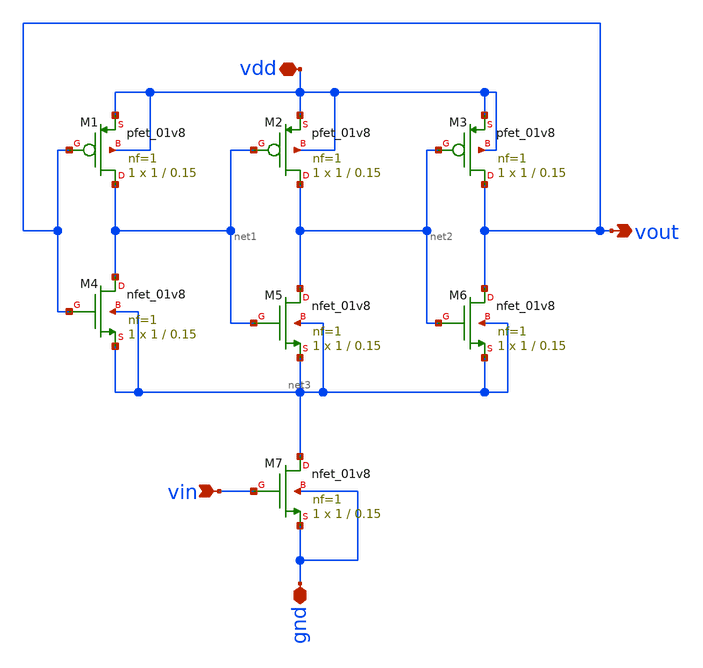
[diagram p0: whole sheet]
** sch_path: Neuron/voltContrOsc/sch/voltContrOsc.sch
**.subckt voltContrOsc gnd vdd vin vout
*.iopin gnd
*.iopin vdd
*.ipin vin
*.opin vout
XM1 net1 vout vdd vdd sky130_fd_pr__pfet_01v8 L=0.15 W=1 nf=1 ad='int((nf+1)/2) * W/nf * 0.29' as='int((nf+2)/2) * W/nf * 0.29'
+ pd='2*int((nf+1)/2) * (W/nf + 0.29)' ps='2*int((nf+2)/2) * (W/nf + 0.29)' nrd='0.29 / W' nrs='0.29 / W'
+ sa=0 sb=0 sd=0 mult=1 m=1
XM2 net2 net1 vdd vdd sky130_fd_pr__pfet_01v8 L=0.15 W=1 nf=1 ad='int((nf+1)/2) * W/nf * 0.29' as='int((nf+2)/2) * W/nf * 0.29'
+ pd='2*int((nf+1)/2) * (W/nf + 0.29)' ps='2*int((nf+2)/2) * (W/nf + 0.29)' nrd='0.29 / W' nrs='0.29 / W'
+ sa=0 sb=0 sd=0 mult=1 m=1
XM3 vout net2 vdd vdd sky130_fd_pr__pfet_01v8 L=0.15 W=1 nf=1 ad='int((nf+1)/2) * W/nf * 0.29' as='int((nf+2)/2) * W/nf * 0.29'
+ pd='2*int((nf+1)/2) * (W/nf + 0.29)' ps='2*int((nf+2)/2) * (W/nf + 0.29)' nrd='0.29 / W' nrs='0.29 / W'
+ sa=0 sb=0 sd=0 mult=1 m=1
XM4 net1 vout net3 net3 sky130_fd_pr__nfet_01v8 L=0.15 W=1 nf=1 ad='int((nf+1)/2) * W/nf * 0.29' as='int((nf+2)/2) * W/nf * 0.29'
+ pd='2*int((nf+1)/2) * (W/nf + 0.29)' ps='2*int((nf+2)/2) * (W/nf + 0.29)' nrd='0.29 / W' nrs='0.29 / W'
+ sa=0 sb=0 sd=0 mult=1 m=1
XM5 net2 net1 net3 net3 sky130_fd_pr__nfet_01v8 L=0.15 W=1 nf=1 ad='int((nf+1)/2) * W/nf * 0.29' as='int((nf+2)/2) * W/nf * 0.29'
+ pd='2*int((nf+1)/2) * (W/nf + 0.29)' ps='2*int((nf+2)/2) * (W/nf + 0.29)' nrd='0.29 / W' nrs='0.29 / W'
+ sa=0 sb=0 sd=0 mult=1 m=1
XM6 vout net2 net3 net3 sky130_fd_pr__nfet_01v8 L=0.15 W=1 nf=1 ad='int((nf+1)/2) * W/nf * 0.29' as='int((nf+2)/2) * W/nf * 0.29'
+ pd='2*int((nf+1)/2) * (W/nf + 0.29)' ps='2*int((nf+2)/2) * (W/nf + 0.29)' nrd='0.29 / W' nrs='0.29 / W'
+ sa=0 sb=0 sd=0 mult=1 m=1
XM7 net3 vin gnd gnd sky130_fd_pr__nfet_01v8 L=0.15 W=1 nf=1 ad='int((nf+1)/2) * W/nf * 0.29' as='int((nf+2)/2) * W/nf * 0.29'
+ pd='2*int((nf+1)/2) * (W/nf + 0.29)' ps='2*int((nf+2)/2) * (W/nf + 0.29)' nrd='0.29 / W' nrs='0.29 / W'
+ sa=0 sb=0 sd=0 mult=1 m=1
**.ends
.end
